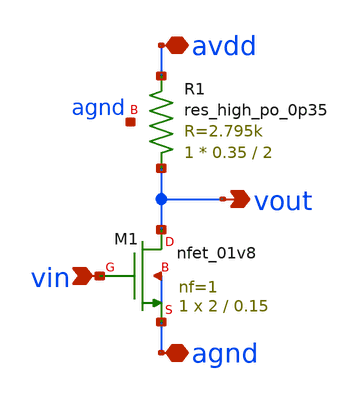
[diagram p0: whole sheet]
** sch_path: AMP/Final_Amp.sch
**.subckt Final_Amp avdd vin vout agnd
*.iopin avdd
*.ipin vin
*.opin vout
*.iopin agnd
XM1 vout vin agnd agnd sky130_fd_pr__nfet_01v8 L=0.15 W=2 nf=1 ad='int((nf+1)/2) * W/nf * 0.29' as='int((nf+2)/2) * W/nf * 0.29'
+ pd='2*int((nf+1)/2) * (W/nf + 0.29)' ps='2*int((nf+2)/2) * (W/nf + 0.29)' nrd='0.29 / W' nrs='0.29 / W'
+ sa=0 sb=0 sd=0 mult=1 m=1
XR1 vout avdd agnd sky130_fd_pr__res_high_po_0p35 L=2 mult=1 m=1
**.ends
.end
